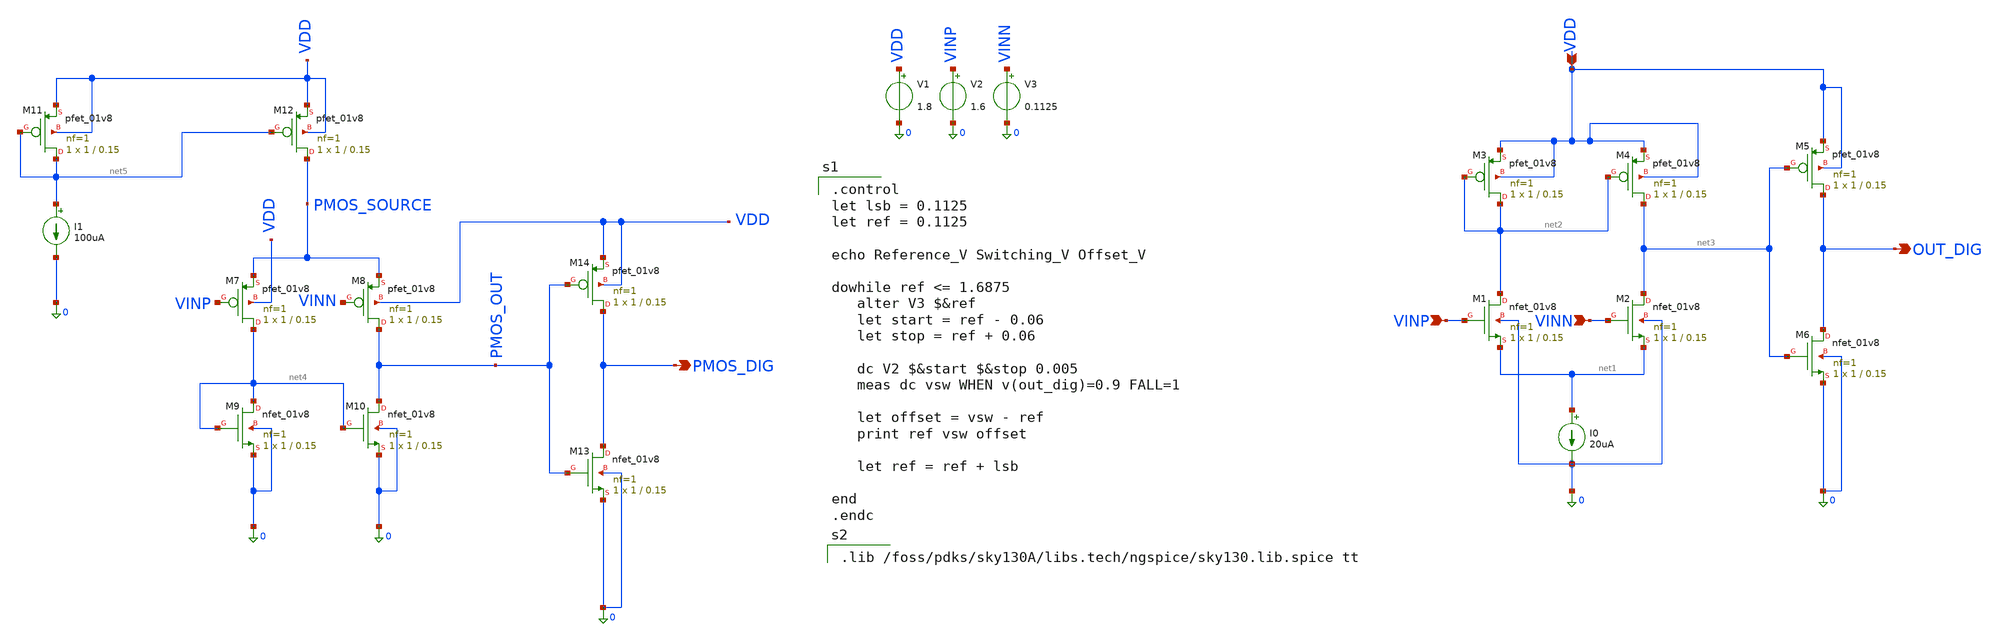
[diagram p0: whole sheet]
** sch_path: comparator_v2.sch
**.subckt comparator_v2 VINP VINN VDD OUT_DIG PMOS_DIG
*.ipin VINP
*.ipin VINN
*.ipin VDD
*.opin OUT_DIG
*.opin PMOS_DIG
I0 net1 0 20uA
XM1 net2 VINP net1 0 sky130_fd_pr__nfet_01v8 L=0.15 W=1 nf=1 ad='int((1 + 1)/2) * 1 / 1 * 0.29' as='int((1 + 2)/2) * 1 / 1 * 0.29'
+ pd='2*int((1 + 1)/2) * (1 / 1 + 0.29)' ps='2*int((1 + 2)/2) * (1 / 1 + 0.29)' nrd='0.29 / 1 ' nrs='0.29 / 1 '
+ sa=0 sb=0 sd=0 mult=1 m=1
XM2 net3 VINN net1 0 sky130_fd_pr__nfet_01v8 L=0.15 W=1 nf=1 ad='int((1 + 1)/2) * 1 / 1 * 0.29' as='int((1 + 2)/2) * 1 / 1 * 0.29'
+ pd='2*int((1 + 1)/2) * (1 / 1 + 0.29)' ps='2*int((1 + 2)/2) * (1 / 1 + 0.29)' nrd='0.29 / 1 ' nrs='0.29 / 1 '
+ sa=0 sb=0 sd=0 mult=1 m=1
XM6 OUT_DIG net3 0 0 sky130_fd_pr__nfet_01v8 L=0.15 W=1 nf=1 ad='int((1 + 1)/2) * 1 / 1 * 0.29' as='int((1 + 2)/2) * 1 / 1 * 0.29'
+ pd='2*int((1 + 1)/2) * (1 / 1 + 0.29)' ps='2*int((1 + 2)/2) * (1 / 1 + 0.29)' nrd='0.29 / 1 ' nrs='0.29 / 1 '
+ sa=0 sb=0 sd=0 mult=1 m=1
XM3 net2 net2 VDD VDD sky130_fd_pr__pfet_01v8 L=0.15 W=1 nf=1 ad='int((1 + 1)/2) * 1 / 1 * 0.29' as='int((1 + 2)/2) * 1 / 1 * 0.29'
+ pd='2*int((1 + 1)/2) * (1 / 1 + 0.29)' ps='2*int((1 + 2)/2) * (1 / 1 + 0.29)' nrd='0.29 / 1 ' nrs='0.29 / 1 '
+ sa=0 sb=0 sd=0 mult=1 m=1
XM4 net3 net2 VDD VDD sky130_fd_pr__pfet_01v8 L=0.15 W=1 nf=1 ad='int((1 + 1)/2) * 1 / 1 * 0.29' as='int((1 + 2)/2) * 1 / 1 * 0.29'
+ pd='2*int((1 + 1)/2) * (1 / 1 + 0.29)' ps='2*int((1 + 2)/2) * (1 / 1 + 0.29)' nrd='0.29 / 1 ' nrs='0.29 / 1 '
+ sa=0 sb=0 sd=0 mult=1 m=1
XM5 OUT_DIG net3 VDD VDD sky130_fd_pr__pfet_01v8 L=0.15 W=1 nf=1 ad='int((1 + 1)/2) * 1 / 1 * 0.29' as='int((1 + 2)/2) * 1 / 1 * 0.29'
+ pd='2*int((1 + 1)/2) * (1 / 1 + 0.29)' ps='2*int((1 + 2)/2) * (1 / 1 + 0.29)' nrd='0.29 / 1 ' nrs='0.29 / 1 '
+ sa=0 sb=0 sd=0 mult=1 m=1
V1 VDD 0 1.8
V2 VINP 0 1.6
V3 VINN 0 0.1125
XM7 net4 VINP PMOS_SOURCE VDD sky130_fd_pr__pfet_01v8 L=0.15 W=1 nf=1 ad='int((1 + 1)/2) * 1 / 1 * 0.29'
+ as='int((1 + 2)/2) * 1 / 1 * 0.29' pd='2*int((1 + 1)/2) * (1 / 1 + 0.29)' ps='2*int((1 + 2)/2) * (1 / 1 + 0.29)'
+ nrd='0.29 / 1 ' nrs='0.29 / 1 ' sa=0 sb=0 sd=0 mult=1 m=1
XM8 PMOS_OUT VINN PMOS_SOURCE VDD sky130_fd_pr__pfet_01v8 L=0.15 W=1 nf=1 ad='int((1 + 1)/2) * 1 / 1 * 0.29'
+ as='int((1 + 2)/2) * 1 / 1 * 0.29' pd='2*int((1 + 1)/2) * (1 / 1 + 0.29)' ps='2*int((1 + 2)/2) * (1 / 1 + 0.29)'
+ nrd='0.29 / 1 ' nrs='0.29 / 1 ' sa=0 sb=0 sd=0 mult=1 m=1
XM9 net4 net4 0 0 sky130_fd_pr__nfet_01v8 L=0.15 W=1 nf=1 ad='int((1 + 1)/2) * 1 / 1 * 0.29' as='int((1 + 2)/2) * 1 / 1 * 0.29'
+ pd='2*int((1 + 1)/2) * (1 / 1 + 0.29)' ps='2*int((1 + 2)/2) * (1 / 1 + 0.29)' nrd='0.29 / 1 ' nrs='0.29 / 1 '
+ sa=0 sb=0 sd=0 mult=1 m=1
XM10 PMOS_OUT net4 0 0 sky130_fd_pr__nfet_01v8 L=0.15 W=1 nf=1 ad='int((1 + 1)/2) * 1 / 1 * 0.29' as='int((1 + 2)/2) * 1 / 1 * 0.29'
+ pd='2*int((1 + 1)/2) * (1 / 1 + 0.29)' ps='2*int((1 + 2)/2) * (1 / 1 + 0.29)' nrd='0.29 / 1 ' nrs='0.29 / 1 '
+ sa=0 sb=0 sd=0 mult=1 m=1
XM11 net5 net5 VDD VDD sky130_fd_pr__pfet_01v8 L=0.15 W=1 nf=1 ad='int((1 + 1)/2) * 1 / 1 * 0.29' as='int((1 + 2)/2) * 1 / 1 * 0.29'
+ pd='2*int((1 + 1)/2) * (1 / 1 + 0.29)' ps='2*int((1 + 2)/2) * (1 / 1 + 0.29)' nrd='0.29 / 1 ' nrs='0.29 / 1 '
+ sa=0 sb=0 sd=0 mult=1 m=1
XM12 PMOS_SOURCE net5 VDD VDD sky130_fd_pr__pfet_01v8 L=0.15 W=1 nf=1 ad='int((1 + 1)/2) * 1 / 1 * 0.29'
+ as='int((1 + 2)/2) * 1 / 1 * 0.29' pd='2*int((1 + 1)/2) * (1 / 1 + 0.29)' ps='2*int((1 + 2)/2) * (1 / 1 + 0.29)'
+ nrd='0.29 / 1 ' nrs='0.29 / 1 ' sa=0 sb=0 sd=0 mult=1 m=1
I1 net5 0 100uA
XM13 PMOS_DIG PMOS_OUT 0 0 sky130_fd_pr__nfet_01v8 L=0.15 W=1 nf=1 ad='int((1 + 1)/2) * 1 / 1 * 0.29'
+ as='int((1 + 2)/2) * 1 / 1 * 0.29' pd='2*int((1 + 1)/2) * (1 / 1 + 0.29)' ps='2*int((1 + 2)/2) * (1 / 1 + 0.29)'
+ nrd='0.29 / 1 ' nrs='0.29 / 1 ' sa=0 sb=0 sd=0 mult=1 m=1
XM14 PMOS_DIG PMOS_OUT VDD VDD sky130_fd_pr__pfet_01v8 L=0.15 W=1 nf=1 ad='int((1 + 1)/2) * 1 / 1 * 0.29'
+ as='int((1 + 2)/2) * 1 / 1 * 0.29' pd='2*int((1 + 1)/2) * (1 / 1 + 0.29)' ps='2*int((1 + 2)/2) * (1 / 1 + 0.29)'
+ nrd='0.29 / 1 ' nrs='0.29 / 1 ' sa=0 sb=0 sd=0 mult=1 m=1
**** begin user architecture code

.control
let lsb = 0.1125
let ref = 0.1125

echo Reference_V Switching_V Offset_V

dowhile ref <= 1.6875
   alter V3 $&ref
   let start = ref - 0.06
   let stop = ref + 0.06

   dc V2 $&start $&stop 0.005
   meas dc vsw WHEN v(out_dig)=0.9 FALL=1

   let offset = vsw - ref
   print ref vsw offset

   let ref = ref + lsb

end
.endc


.lib /foss/pdks/sky130A/libs.tech/ngspice/sky130.lib.spice tt

**** end user architecture code
**.ends
.end
